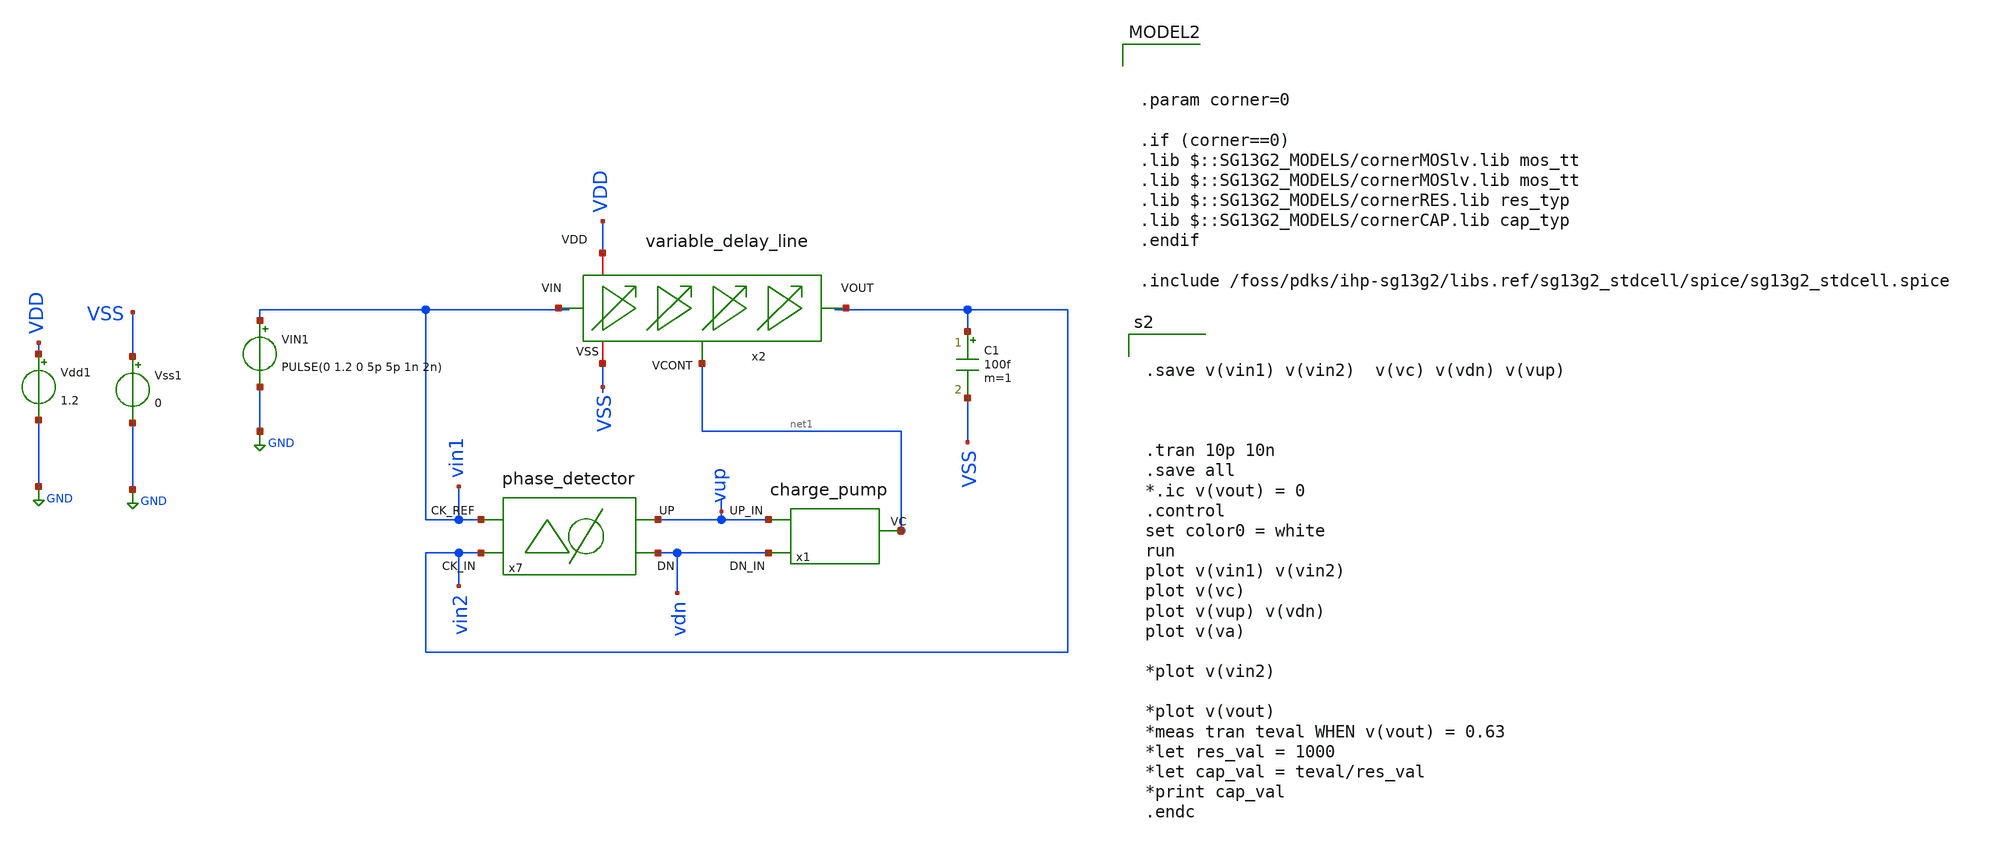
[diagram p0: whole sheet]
** sch_path: xschem/DLL/DLL_tb_top.sch
* IHP-GmbH/IHP-Open-PDK/ihp-sg13g2/libs.tech/xschem/sg13g2_stdcells/sg13g2_dlygate4sd2_1.sch:
* Copyright 2023 IHP PDK Authors
* Licensed under the Apache License, Version 2.0 (the "License");
**.subckt DLL_tb_top
C1 vin2 VSS 100f m=1
VIN1 vin1 GND PULSE(0 1.2 0 5p 5p 1n 2n)
Vss1 VSS GND 0
x7 vin2 vup vin1 vdn phase_detector
x2 VDD VSS net1 net2 net3 variable_delay_line
Vdd1 VDD GND 1.2
x1 vup net1 vdn charge_pump
**** begin user architecture code


.save v(vin1) v(vin2)  v(vc) v(vdn) v(vup)



.tran 10p 10n
.save all
*.ic v(vout) = 0
.control
set color0 = white
run
plot v(vin1) v(vin2)
plot v(vc)
plot v(vup) v(vdn)
plot v(va)

*plot v(vin2)

*plot v(vout)
*meas tran teval WHEN v(vout) = 0.63
*let res_val = 1000
*let cap_val = teval/res_val
*print cap_val
.endc




.param corner=0

.if (corner==0)
.lib $::SG13G2_MODELS/cornerMOSlv.lib mos_tt
.lib $::SG13G2_MODELS/cornerMOSlv.lib mos_tt
.lib $::SG13G2_MODELS/cornerRES.lib res_typ
.lib $::SG13G2_MODELS/cornerCAP.lib cap_typ
.endif

.include /foss/pdks/ihp-sg13g2/libs.ref/sg13g2_stdcell/spice/sg13g2_stdcell.spice

**** end user architecture code
**.ends

* expanding   symbol:  /foss/designs/UNIC-CASS-Aug25/sch/phase_detector/phase_detector.sym # of
*+ pins=4
** sym_path: xschem/phase_detector/phase_detector.sym
** sch_path: xschem/phase_detector/phase_detector.sch
.subckt phase_detector CK_IN UP CK_REF DN
*.opin UP
*.ipin CK_IN
*.ipin CK_REF
*.opin DN
XM7 net2 CK_IN VDD VDD sg13_lv_pmos w=5u l=4u ng=1 m=1 mm_ok=1
XM8 net1 CK_IN VDD VDD sg13_lv_pmos w=5u l=4u ng=1 m=1 mm_ok=1
XM9 net2 CK_REF net1 net1 sg13_lv_nmos w=2u l=5u ng=5 m=1 mm_ok=1
XM10 net2 DN net1 VSS sg13_lv_nmos w=2u l=5u ng=5 m=1 mm_ok=1
XM11 net1 CK_IN VSS VSS sg13_lv_nmos w=2u l=5u ng=5 m=1 mm_ok=1
XM6 UP net2 VDD VDD sg13_lv_pmos w=5u l=4u ng=1 m=1 mm_ok=1
XM12 UP CK_IN net3 net4 sg13_lv_nmos w=2u l=5u ng=5 m=1 mm_ok=1
XM13 net3 net2 net4 net4 sg13_lv_nmos w=2u l=5u ng=5 m=1 mm_ok=1
XM14 net3 net2 VDD VDD sg13_lv_pmos w=5u l=4u ng=1 m=1 mm_ok=1
XM19 net6 CK_IN VDD VDD sg13_lv_pmos w=5u l=4u ng=1 m=1 mm_ok=1
XM20 net5 CK_IN VDD VDD sg13_lv_pmos w=5u l=4u ng=1 m=1 mm_ok=1
XM21 net6 CK_REF net5 net5 sg13_lv_nmos w=2u l=5u ng=5 m=1 mm_ok=1
XM22 net6 UP net5 VSS sg13_lv_nmos w=2u l=5u ng=5 m=1 mm_ok=1
XM23 net5 CK_IN VSS VSS sg13_lv_nmos w=2u l=5u ng=5 m=1 mm_ok=1
XM24 DN net6 VDD VDD sg13_lv_pmos w=5u l=4u ng=1 m=1 mm_ok=1
XM25 DN CK_REF net7 net8 sg13_lv_nmos w=2u l=5u ng=5 m=1 mm_ok=1
XM26 net7 net6 net8 net8 sg13_lv_nmos w=2u l=5u ng=5 m=1 mm_ok=1
XM27 net7 net6 VDD VDD sg13_lv_pmos w=5u l=4u ng=1 m=1 mm_ok=1
.ends


* expanding   symbol:  /foss/designs/UNIC-CASS-Aug25/sch/delay_variable_line/variable_delay_line.sym
*+ # of pins=5
** sym_path: xschem/delay_variable_line/variable_delay_line.sym
** sch_path: xschem/delay_variable_line/variable_delay_line.sch
.subckt variable_delay_line VDD VSS VCONT VOUT VIN
*.iopin VSS
*.iopin VDD
*.ipin VIN
*.opin VOUT
*.ipin VCONT
x1 VDD VIN va VCONT VSS delay_variable
x2 VDD VSS va VOUT large_delay_vto1p1
.ends


* expanding   symbol:  /foss/designs/UNIC-CASS-Aug25/sch/charge_pump/charge_pump.sym # of pins=3
** sym_path: xschem/charge_pump/charge_pump.sym
** sch_path: xschem/charge_pump/charge_pump.sch
.subckt charge_pump UP_IN VC DN_IN
*.opin VC
*.ipin UP_IN
*.ipin DN_IN
XM1 net1 DN_IN net2 VSS sg13_lv_nmos w=0.3u l=0.45u ng=1 m=1 mm_ok=1
XM7 net1 net1 VDD VDD sg13_lv_pmos w=0.15u l=0.13u ng=1 m=1 mm_ok=1
XM2 net7 DNB net2 VSS sg13_lv_nmos w=0.3u l=0.45u ng=1 m=1 mm_ok=1
XM3 net2 VDD VSS VSS sg13_lv_nmos w=0.3u l=0.45u ng=1 m=1 mm_ok=1
XM4 net1 net1 VDD VDD sg13_lv_pmos w=0.15u l=0.13u ng=1 m=1 mm_ok=1
XM5 net5 net7 VDD VDD sg13_lv_pmos w=0.15u l=0.13u ng=1 m=1 mm_ok=1
XM6 net4 UPB net3 VSS sg13_lv_nmos w=0.3u l=0.45u ng=1 m=1 mm_ok=1
XM8 net6 net4 VDD VDD sg13_lv_pmos w=0.15u l=0.13u ng=1 m=1 mm_ok=1
XM9 VC UP_IN net3 VSS sg13_lv_nmos w=0.3u l=0.45u ng=1 m=1 mm_ok=1
XM10 net3 VDD VSS VSS sg13_lv_nmos w=0.3u l=0.45u ng=1 m=1 mm_ok=1
XM11 VC net1 VDD VDD sg13_lv_pmos w=0.15u l=0.13u ng=1 m=1 mm_ok=1
XM12 VC net1 VDD VDD sg13_lv_pmos w=0.15u l=0.13u ng=1 m=1 mm_ok=1
XM13 net6 net4 VDD VDD sg13_lv_pmos w=0.15u l=0.13u ng=1 m=1 mm_ok=1
XM14 net5 net7 VDD VDD sg13_lv_pmos w=0.15u l=0.13u ng=1 m=1 mm_ok=1
C1 VC VSS 10f m=1
x1 VDD DN_IN DNB VSS inv_1_manual
x2 VDD UP_IN UPB VSS inv_1_manual
.ends


* expanding   symbol:  /foss/designs/UNIC-CASS-Aug25/sch/inv_1_manual/inv_1_manual.sym # of pins=4
** sym_path: xschem/inv_1_manual/inv_1_manual.sym
** sch_path: xschem/inv_1_manual/inv_1_manual.sch
.subckt inv_1_manual VDD_D A Y VSS_D
*.iopin VDD_D
*.iopin VSS_D
*.iopin A
*.iopin Y
XM1 Y A VSS_D VSS_D sg13_lv_nmos w=10u l=0.13u ng=1 m=1 mm_ok=1
XM2 Y A VDD_D VDD_D sg13_lv_pmos w=10u l=0.13u ng=1 m=1 mm_ok=1
.ends


* expanding   symbol:  /foss/designs/UNIC-CASS-Aug25/sch/delay_variable/delay_variable.sym # of
*+ pins=5
** sym_path: xschem/delay_variable/delay_variable.sym
** sch_path: xschem/delay_variable/delay_variable.sch
.subckt delay_variable VDD_D VIN_D VOUT_D VCONT_D VSS_D
*.iopin VSS_D
*.iopin VDD_D
*.opin VOUT_D
*.ipin VCONT_D
*.ipin VIN_D
XM3 net3 VCONT_D VSS_D VSS_D sg13_lv_nmos w=1u l=0.13u ng=1 m=1 mm_ok=1
XM5 net2 VCONT_D VSS_D VSS_D sg13_lv_nmos w=2u l=2u ng=1 m=1 mm_ok=1
XM4 net3 net3 VDD_D VDD_D sg13_lv_pmos w=2.24u l=0.13u ng=1 m=1 mm_ok=1
XM6 net1 net3 VDD_D VDD_D sg13_lv_pmos w=4u l=2u ng=1 m=1 mm_ok=1
XM7 VOUT_D VIN_D net1 VDD_D sg13_lv_pmos w=20u l=2u ng=4 m=1 mm_ok=1
XM8 VOUT_D VIN_D net2 VSS_D sg13_lv_nmos w=5u l=3u ng=1 m=1 mm_ok=1
.ends


* expanding   symbol:  /foss/designs/UNIC-CASS-Aug25/sch/large_delay_vto1p1/large_delay_vto1p1.sym #
*+ of pins=4
** sym_path: xschem/large_delay_vto1p1/large_delay_vto1p1.sym
** sch_path: xschem/large_delay_vto1p1/large_delay_vto1p1.sch
.subckt large_delay_vto1p1 VCC VSS VIN VOUT
*.iopin VIN
*.iopin VOUT
*.iopin VCC
*.iopin VSS
x1 VOUT VIN VCC VSS sg13g2_dlygate4sd2_1
x2 VOUT VIN VCC VSS sg13g2_dlygate4sd2_1
x3 VOUT VIN VCC VSS sg13g2_dlygate4sd2_1
x10 VOUT VIN VCC VSS sg13g2_dlygate4sd2_1
.ends


* expanding   symbol:  sg13g2_stdcells/sg13g2_dlygate4sd3_1.sym # of pins=2
** sym_path: sg13g2_stdcells/sg13g2_dlygate4sd3_1.sym
** sch_path: sg13g2_stdcells/sg13g2_dlygate4sd3_1.sch
.subckt sg13g2_dlygate4sd3_1 X A VDD VSS
*.ipin A
*.opin X
*.iopin VDD
*.iopin VSS
XM1 net3 A VSS VSS sg13_lv_nmos w=420.00n l=130.00n ng=1 m=1 mm_ok=1
XM2 net1 net3 VSS VSS sg13_lv_nmos w=420.00n l=500.0n ng=1 m=1 mm_ok=1
XM3 net2 net1 VSS VSS sg13_lv_nmos w=420.00n l=500.0n ng=1 m=1 mm_ok=1
XM4 X net2 VSS VSS sg13_lv_nmos w=740.00n l=130.00n ng=1 m=1 mm_ok=1
XM5 net3 A VDD VDD sg13_lv_pmos w=420.00n l=130.00n ng=1 m=1 mm_ok=1
XM6 net1 net3 VDD VDD sg13_lv_pmos w=1.000u l=500.0n ng=1 m=1 mm_ok=1
XM7 net2 net1 VDD VDD sg13_lv_pmos w=1.000u l=500.0n ng=1 m=1 mm_ok=1
XM8 X net2 VDD VDD sg13_lv_pmos w=1.12u l=130.00n ng=1 m=1 mm_ok=1
.ends


* expanding   symbol:  sg13g2_stdcells/sg13g2_dlygate4sd2_1.sym # of pins=2
** sym_path: sg13g2_stdcells/sg13g2_dlygate4sd2_1.sym
** sch_path: sg13g2_stdcells/sg13g2_dlygate4sd2_1.sch
.subckt sg13g2_dlygate4sd2_1 X A VDD VSS
*.ipin A
*.opin X
*.iopin VDD
*.iopin VSS
XM1 net2 A VSS VSS sg13_lv_nmos w=420.00n l=130.00n ng=1 m=1 mm_ok=1
XM2 net1 net2 VSS VSS sg13_lv_nmos w=420.00n l=180.00n ng=1 m=1 mm_ok=1
XM3 net3 net1 VSS VSS sg13_lv_nmos w=420.00n l=180.00n ng=1 m=1 mm_ok=1
XM4 X net3 VSS VSS sg13_lv_nmos w=740.00n l=130.00n ng=1 m=1 mm_ok=1
XM5 net2 A VDD VDD sg13_lv_pmos w=420.00n l=130.00n ng=1 m=1 mm_ok=1
XM6 net1 net2 VDD VDD sg13_lv_pmos w=1.000u l=250.00n ng=1 m=1 mm_ok=1
XM7 net3 net1 VDD VDD sg13_lv_pmos w=1.000u l=250.00n ng=1 m=1 mm_ok=1
XM8 X net3 VDD VDD sg13_lv_pmos w=1.12u l=130.00n ng=1 m=1 mm_ok=1
.ends

.GLOBAL GND
.end
